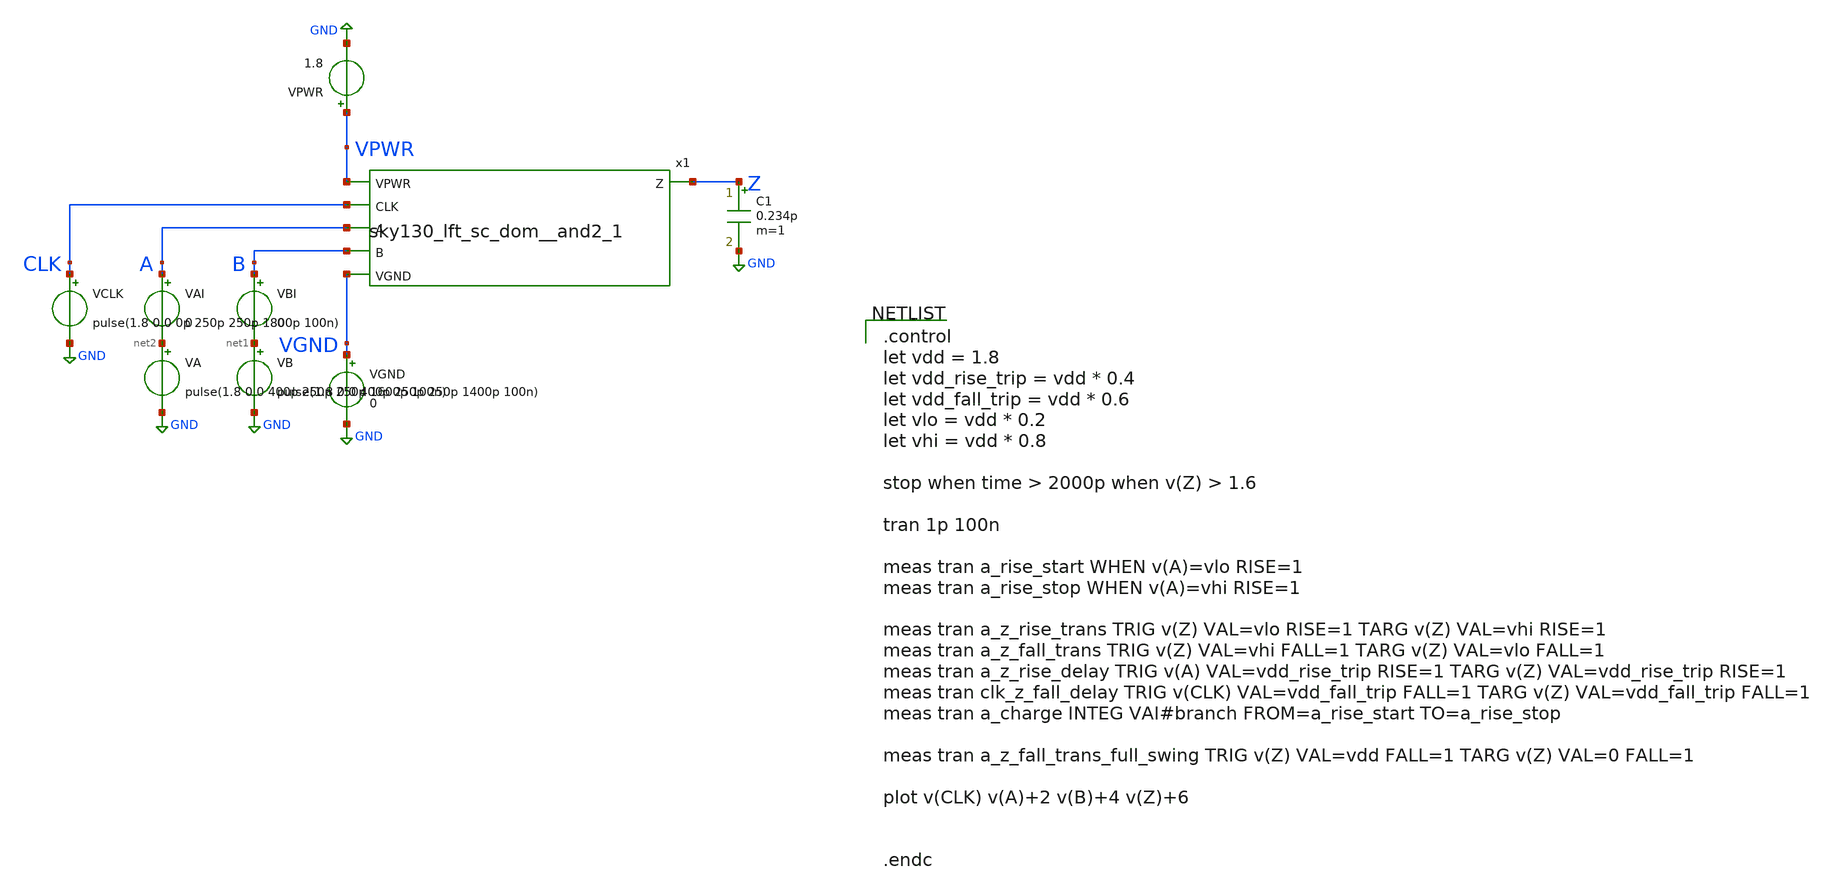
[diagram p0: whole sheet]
** sch_path: cells/xschem/sky130_lft_sc_dom__and2_1_tb.sch
**.subckt sky130_lft_sc_dom__and2_1_tb
x1 VPWR CLK Z A B VGND sky130_lft_sc_dom__and2_1
VGND VGND GND 0
VPWR VPWR GND 1.8
VB net1 GND pulse(1.8 0.0 400p 250p 250p 1400p 100n)
VA net2 GND pulse(1.8 0.0 400p 250p 250p 1600p 100n)
VCLK CLK GND pulse(1.8 0.0 0p 250p 250p 1800p 100n)
VBI B net1 0
VAI A net2 0
C1 Z GND 0.234p m=1
**** begin user architecture code

** opencircuitdesign pdks install
.lib $::SKYWATER_MODELS/sky130.lib.spice ss


.control
let vdd = 1.8
let vdd_rise_trip = vdd * 0.4
let vdd_fall_trip = vdd * 0.6
let vlo = vdd * 0.2
let vhi = vdd * 0.8

stop when time > 2000p when v(Z) > 1.6

tran 1p 100n

meas tran a_rise_start WHEN v(A)=vlo RISE=1
meas tran a_rise_stop WHEN v(A)=vhi RISE=1

meas tran a_z_rise_trans TRIG v(Z) VAL=vlo RISE=1 TARG v(Z) VAL=vhi RISE=1
meas tran a_z_fall_trans TRIG v(Z) VAL=vhi FALL=1 TARG v(Z) VAL=vlo FALL=1
meas tran a_z_rise_delay TRIG v(A) VAL=vdd_rise_trip RISE=1 TARG v(Z) VAL=vdd_rise_trip RISE=1
meas tran clk_z_fall_delay TRIG v(CLK) VAL=vdd_fall_trip FALL=1 TARG v(Z) VAL=vdd_fall_trip FALL=1
meas tran a_charge INTEG VAI#branch FROM=a_rise_start TO=a_rise_stop

meas tran a_z_fall_trans_full_swing TRIG v(Z) VAL=vdd FALL=1 TARG v(Z) VAL=0 FALL=1

plot v(CLK) v(A)+2 v(B)+4 v(Z)+6


.endc

**** end user architecture code
**.ends

* expanding   symbol:  sky130_lft_sc_dom__and2_1.sym # of pins=6
** sym_path: cells/xschem/sky130_lft_sc_dom__and2_1.sym
** sch_path: cells/xschem/sky130_lft_sc_dom__and2_1.sch
.subckt sky130_lft_sc_dom__and2_1 VPWR CLK Z A B VGND
*.ipin A
*.ipin B
*.ipin CLK
*.ipin VPWR
*.ipin VGND
*.opin Z
XM1 N0 CLK VPWR VPWR sky130_fd_pr__pfet_01v8 L=0.15 W=0.84 nf=1 ad='int((1 + 1)/2) * 0.84 / 1 * 0.29'
+ as='int((1 + 2)/2) * 0.84 / 1 * 0.29' pd='2*int((1 + 1)/2) * (0.84 / 1 + 0.29)' ps='2*int((1 + 2)/2) * (0.84 / 1 + 0.29)'
+ nrd='0.29 / 0.84 ' nrs='0.29 / 0.84 ' sa=0 sb=0 sd=0 mult=1 m=1
XM2 N0 A net2 VGND sky130_fd_pr__nfet_01v8 L=0.15 W=2.52 nf=1 ad='int((1 + 1)/2) * 2.52 / 1 * 0.29' as='int((1 + 2)/2) * 2.52 / 1 * 0.29'
+ pd='2*int((1 + 1)/2) * (2.52 / 1 + 0.29)' ps='2*int((1 + 2)/2) * (2.52 / 1 + 0.29)' nrd='0.29 / 2.52 '
+ nrs='0.29 / 2.52 ' sa=0 sb=0 sd=0 mult=1 m=1
XM3 net2 B net1 VGND sky130_fd_pr__nfet_01v8 L=0.15 W=2.52 nf=1 ad='int((1 + 1)/2) * 2.52 / 1 * 0.29'
+ as='int((1 + 2)/2) * 2.52 / 1 * 0.29' pd='2*int((1 + 1)/2) * (2.52 / 1 + 0.29)' ps='2*int((1 + 2)/2) * (2.52 / 1 + 0.29)'
+ nrd='0.29 / 2.52 ' nrs='0.29 / 2.52 ' sa=0 sb=0 sd=0 mult=1 m=1
XM4 net1 CLK VGND VGND sky130_fd_pr__nfet_01v8 L=0.15 W=2.52 nf=1 ad='int((1 + 1)/2) * 2.52 / 1 * 0.29'
+ as='int((1 + 2)/2) * 2.52 / 1 * 0.29' pd='2*int((1 + 1)/2) * (2.52 / 1 + 0.29)' ps='2*int((1 + 2)/2) * (2.52 / 1 + 0.29)'
+ nrd='0.29 / 2.52 ' nrs='0.29 / 2.52 ' sa=0 sb=0 sd=0 mult=1 m=1
XM6 Z N0 VGND VGND sky130_fd_pr__nfet_01v8 L=0.15 W=0.42 nf=1 ad='int((1 + 1)/2) * 0.42 / 1 * 0.29' as='int((1 + 2)/2) * 0.42 / 1 * 0.29'
+ pd='2*int((1 + 1)/2) * (0.42 / 1 + 0.29)' ps='2*int((1 + 2)/2) * (0.42 / 1 + 0.29)' nrd='0.29 / 0.42 '
+ nrs='0.29 / 0.42 ' sa=0 sb=0 sd=0 mult=1 m=1
XM7 Z N0 VPWR VPWR sky130_fd_pr__pfet_01v8 L=0.15 W=1.68 nf=1 ad='int((1 + 1)/2) * 1.68 / 1 * 0.29' as='int((1 + 2)/2) * 1.68 / 1 * 0.29'
+ pd='2*int((1 + 1)/2) * (1.68 / 1 + 0.29)' ps='2*int((1 + 2)/2) * (1.68 / 1 + 0.29)' nrd='0.29 / 1.68 '
+ nrs='0.29 / 1.68 ' sa=0 sb=0 sd=0 mult=1 m=1
XM8 N0 Z VPWR VPWR sky130_fd_pr__pfet_01v8 L=0.15 W=0.42 nf=1 ad='int((1 + 1)/2) * 0.42 / 1 * 0.29' as='int((1 + 2)/2) * 0.42 / 1 * 0.29'
+ pd='2*int((1 + 1)/2) * (0.42 / 1 + 0.29)' ps='2*int((1 + 2)/2) * (0.42 / 1 + 0.29)' nrd='0.29 / 0.42 '
+ nrs='0.29 / 0.42 ' sa=0 sb=0 sd=0 mult=1 m=1
.ends

.GLOBAL GND
.end
